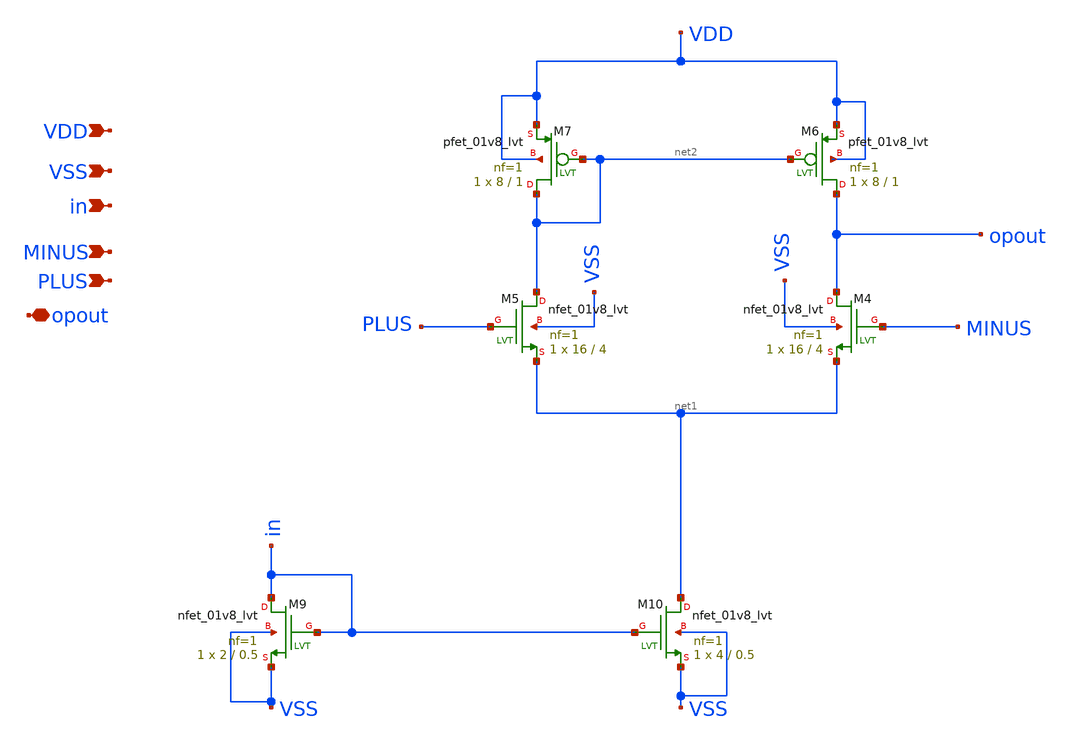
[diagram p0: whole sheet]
** sch_path: custom_gds/tt_um_bgr_agolmanesh/xschem/opamp_l.sch
**.subckt opamp_l VDD VSS in MINUS PLUS opout
*.ipin VDD
*.ipin VSS
*.ipin in
*.ipin MINUS
*.ipin PLUS
*.iopin opout
XM4 opout MINUS net1 VSS sky130_fd_pr__nfet_01v8_lvt L=4 W=16 nf=1 ad='int((nf+1)/2) * W/nf * 0.29' as='int((nf+2)/2) * W/nf * 0.29'
+ pd='2*int((nf+1)/2) * (W/nf + 0.29)' ps='2*int((nf+2)/2) * (W/nf + 0.29)' nrd='0.29 / W' nrs='0.29 / W'
+ sa=0 sb=0 sd=0 mult=1 m=1
XM5 net2 PLUS net1 VSS sky130_fd_pr__nfet_01v8_lvt L=4 W=16 nf=1 ad='int((nf+1)/2) * W/nf * 0.29' as='int((nf+2)/2) * W/nf * 0.29'
+ pd='2*int((nf+1)/2) * (W/nf + 0.29)' ps='2*int((nf+2)/2) * (W/nf + 0.29)' nrd='0.29 / W' nrs='0.29 / W'
+ sa=0 sb=0 sd=0 mult=1 m=1
XM6 opout net2 VDD VDD sky130_fd_pr__pfet_01v8_lvt L=1 W=8 nf=1 ad='int((nf+1)/2) * W/nf * 0.29' as='int((nf+2)/2) * W/nf * 0.29'
+ pd='2*int((nf+1)/2) * (W/nf + 0.29)' ps='2*int((nf+2)/2) * (W/nf + 0.29)' nrd='0.29 / W' nrs='0.29 / W'
+ sa=0 sb=0 sd=0 mult=1 m=1
XM10 net1 in VSS VSS sky130_fd_pr__nfet_01v8_lvt L=0.5 W=4 nf=1 ad='int((nf+1)/2) * W/nf * 0.29' as='int((nf+2)/2) * W/nf * 0.29'
+ pd='2*int((nf+1)/2) * (W/nf + 0.29)' ps='2*int((nf+2)/2) * (W/nf + 0.29)' nrd='0.29 / W' nrs='0.29 / W'
+ sa=0 sb=0 sd=0 mult=1 m=1
XM9 in in VSS VSS sky130_fd_pr__nfet_01v8_lvt L=0.5 W=2 nf=1 ad='int((nf+1)/2) * W/nf * 0.29' as='int((nf+2)/2) * W/nf * 0.29'
+ pd='2*int((nf+1)/2) * (W/nf + 0.29)' ps='2*int((nf+2)/2) * (W/nf + 0.29)' nrd='0.29 / W' nrs='0.29 / W'
+ sa=0 sb=0 sd=0 mult=1 m=1
XM7 net2 net2 VDD VDD sky130_fd_pr__pfet_01v8_lvt L=1 W=8 nf=1 ad='int((nf+1)/2) * W/nf * 0.29' as='int((nf+2)/2) * W/nf * 0.29'
+ pd='2*int((nf+1)/2) * (W/nf + 0.29)' ps='2*int((nf+2)/2) * (W/nf + 0.29)' nrd='0.29 / W' nrs='0.29 / W'
+ sa=0 sb=0 sd=0 mult=1 m=1
**** begin user architecture code

** opencircuitdesign pdks install
.lib $::SKYWATER_MODELS/sky130.lib.spice tt


**** end user architecture code
**.ends
.end
